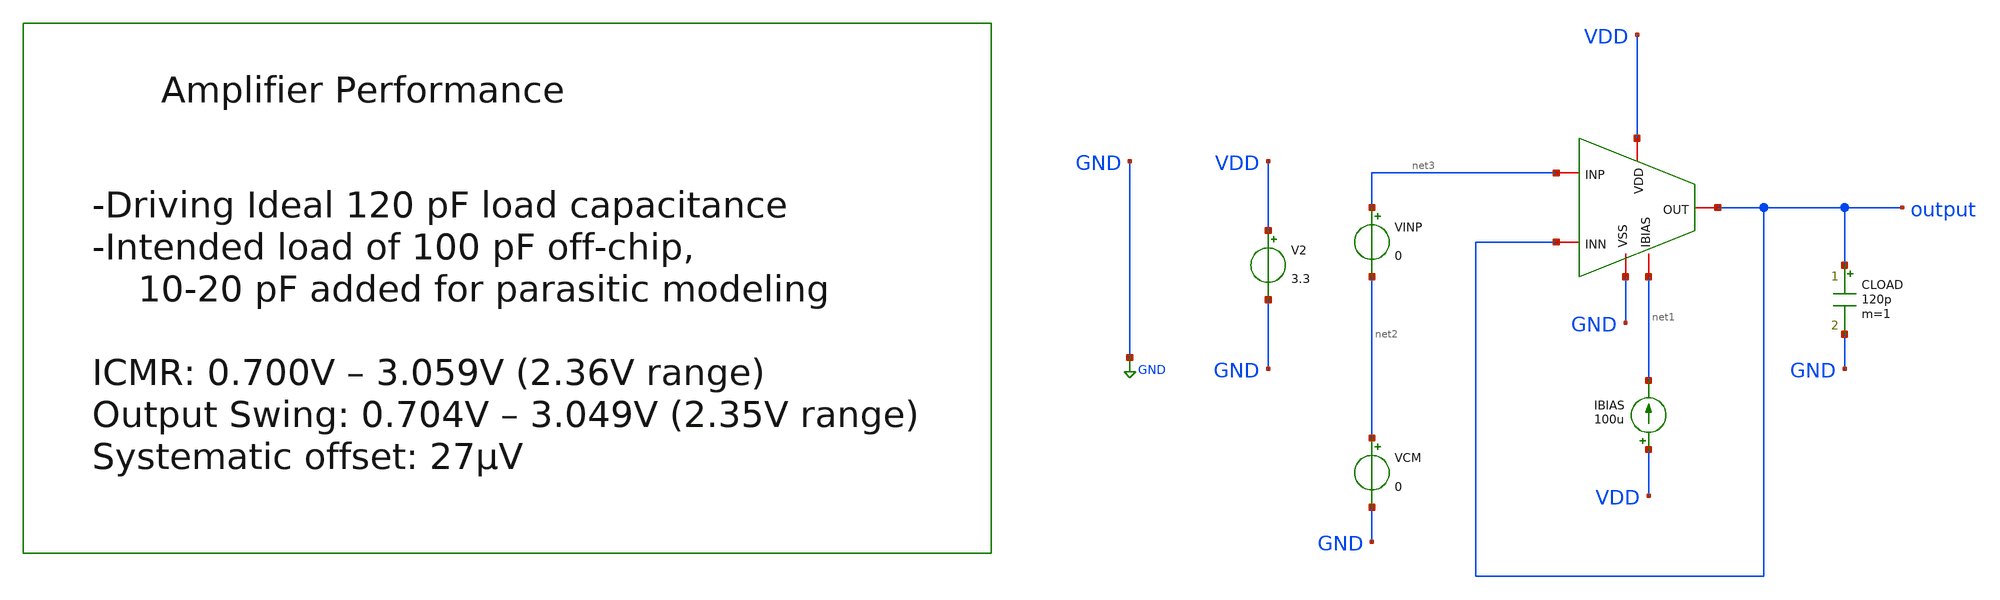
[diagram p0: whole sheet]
** sch_path: designs/libs/core_amps/ota_folded_cascode/tb/dc_unity_tb.sch
**.subckt dc_unity_tb
IBIAS VDD net1 100u
V2 VDD GND 3.3
CLOAD output GND 120p m=1
VINP net3 net2 0
VCM net2 GND 0
x1 VDD GND output net3 output net1 ota_folded_cascode
**** begin user architecture code

.include $::180MCU_MODELS/design.ngspice
.lib $::180MCU_MODELS/sm141064.ngspice typical



.control

set color0=white
set color1=black
set color2=red
set color3=blue

dc VINP 0 4 0.001
let gain = deriv(v(output))
meas dc icmr_low when gain = 0.95 rise = 1
meas dc icmr_high when gain = 0.95 fall = 1
print icmr_low icmr_high
print icmr_high - icmr_low
meas dc out_swing_low find v(output) when gain = 0.95 rise = 1
meas dc out_swing_high find v(output) when gain = 0.95 fall = 1
print out_swing_low out_swing_high
print out_swing_high - out_swing_low
plot v(output) gain
meas dc vos find v(output) at=1.65
let offset = vos - 1.65
print offset

.endc


**** end user architecture code
**.ends
.GLOBAL GND
.end
